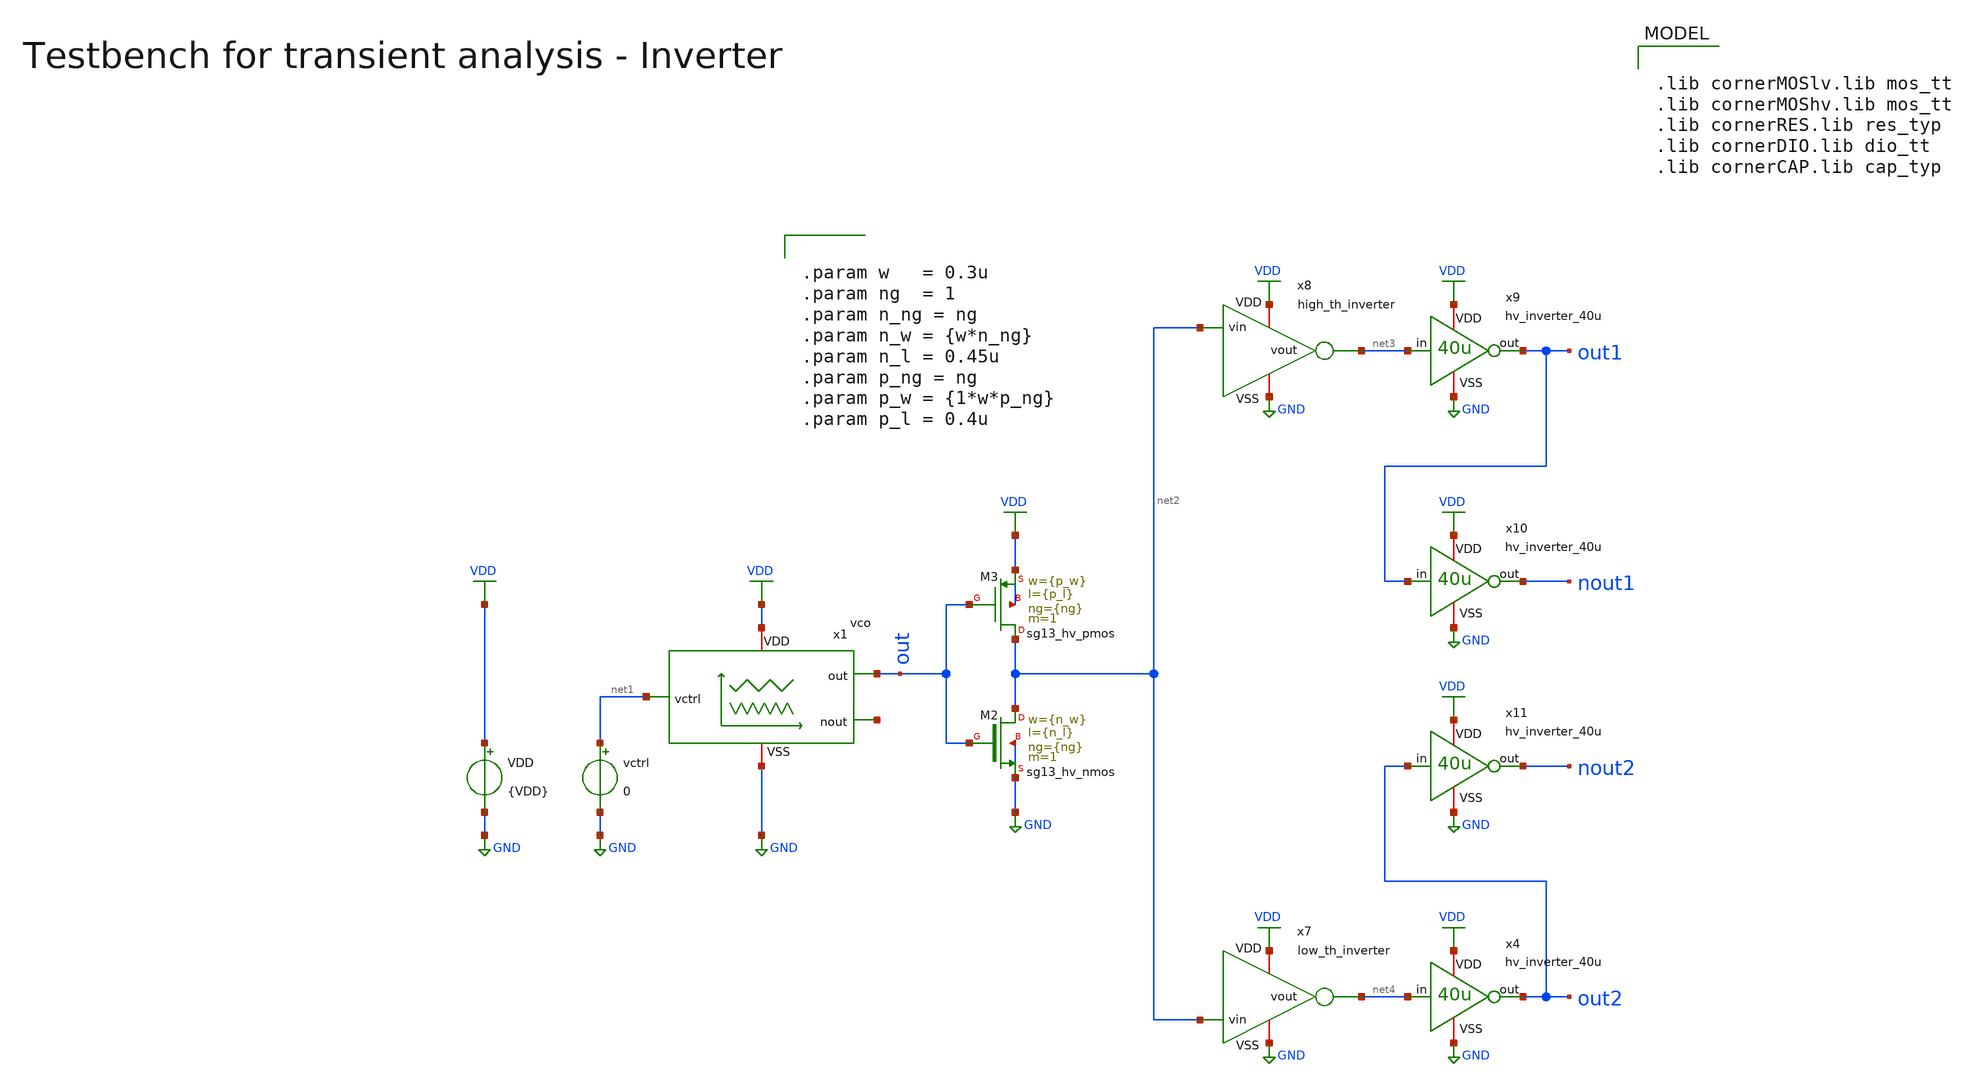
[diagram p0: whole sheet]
** sch_path: macros/heichips26_vcr/macros/switched_capacitor/testbenches/xschem/tb_vco_tran.sch
**.subckt tb_vco_tran
VDD VDD GND {VDD}
vctrl net1 GND 0
x1 VDD out net1 GND net5 vco
XM2 net2 out GND GND sg13_hv_nmos w={n_w} l={n_l} ng={ng} m=1 mm_ok=1
XM3 net2 out VDD VDD sg13_hv_pmos w={p_w} l={p_l} ng={ng} m=1 mm_ok=1
x4 VDD net4 out2 GND hv_inverter_40u
x7 VDD net2 net4 GND low_th_inverter
x8 VDD net2 net3 GND high_th_inverter
x9 VDD net3 out1 GND hv_inverter_40u
x10 VDD out1 nout1 GND hv_inverter_40u
x11 VDD out2 nout2 GND hv_inverter_40u
**** begin user architecture code


.param VDD=3.3
.csparam VDD=VDD
.param Vcm=VDD/2
.param temp=27
.param Cload=10p
.param Rload=1k

.param period = 50n
.param ton    = {period*2}
.csparam tstop  = {2*period}
.csparam tstep  = {period/100}

.options savecurrents klu method=gear reltol=1e-4 abstol=1e-15 gmin=1e-15

.control

save all

* Operating Point Analysis
op
remzerovec
write @schname\.raw
set appendwrite

* Transient Analysis
tran {$&tstep} {$&tstop}
write @schname\.raw

* Plotting
*plot vc+12 thl+12 thh+12 s+8 r+4 vout
*plot vc thl thh vout
plot out
plot out1+4 out2+4 nout1 nout2

* Write Data
unset appendwrite
set wr_vecnames
set wr_singlescale
*wrdata ../plot_simulations/data/@schname\.txt v(vin1) v(vin2) v(vout)

*quit
.endc



.lib cornerMOSlv.lib mos_tt
.lib cornerMOShv.lib mos_tt
.lib cornerRES.lib res_typ
.lib cornerDIO.lib dio_tt
.lib cornerCAP.lib cap_typ



.param w   = 0.3u
.param ng  = 1
.param n_ng = ng
.param n_w = {w*n_ng}
.param n_l = 0.45u
.param p_ng = ng
.param p_w = {1*w*p_ng}
.param p_l = 0.4u


**** end user architecture code
**.ends
.GLOBAL VDD
.GLOBAL GND
.end
